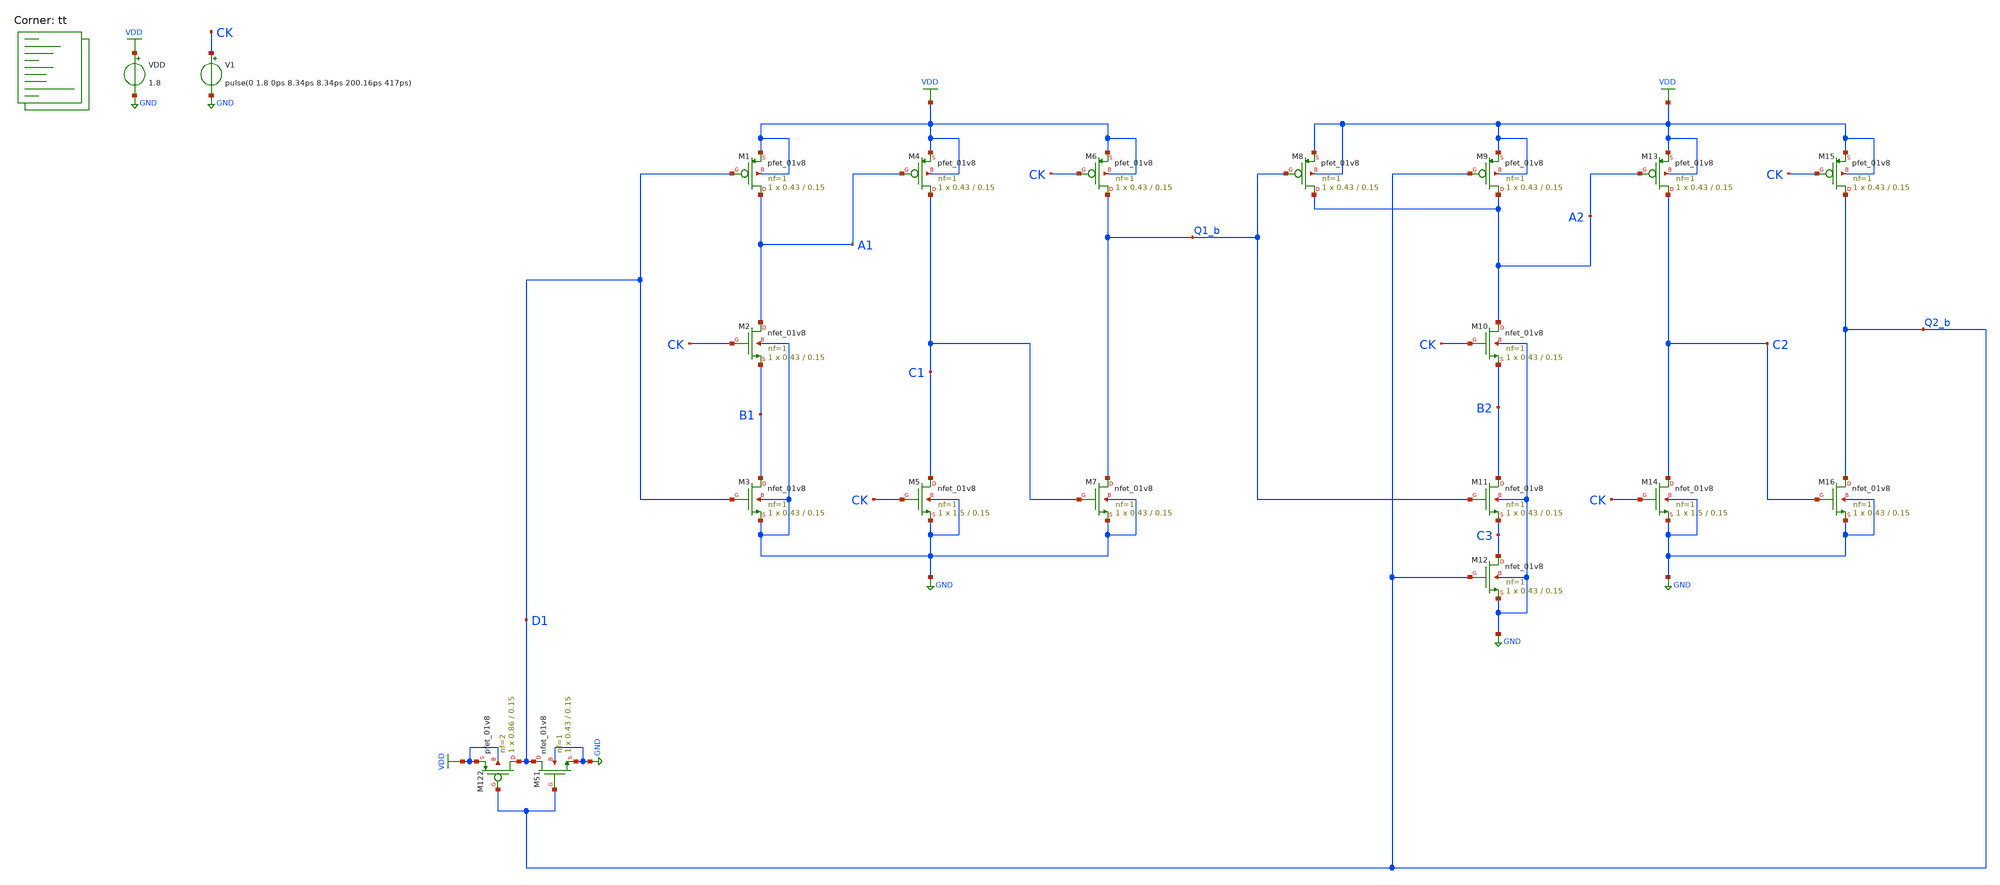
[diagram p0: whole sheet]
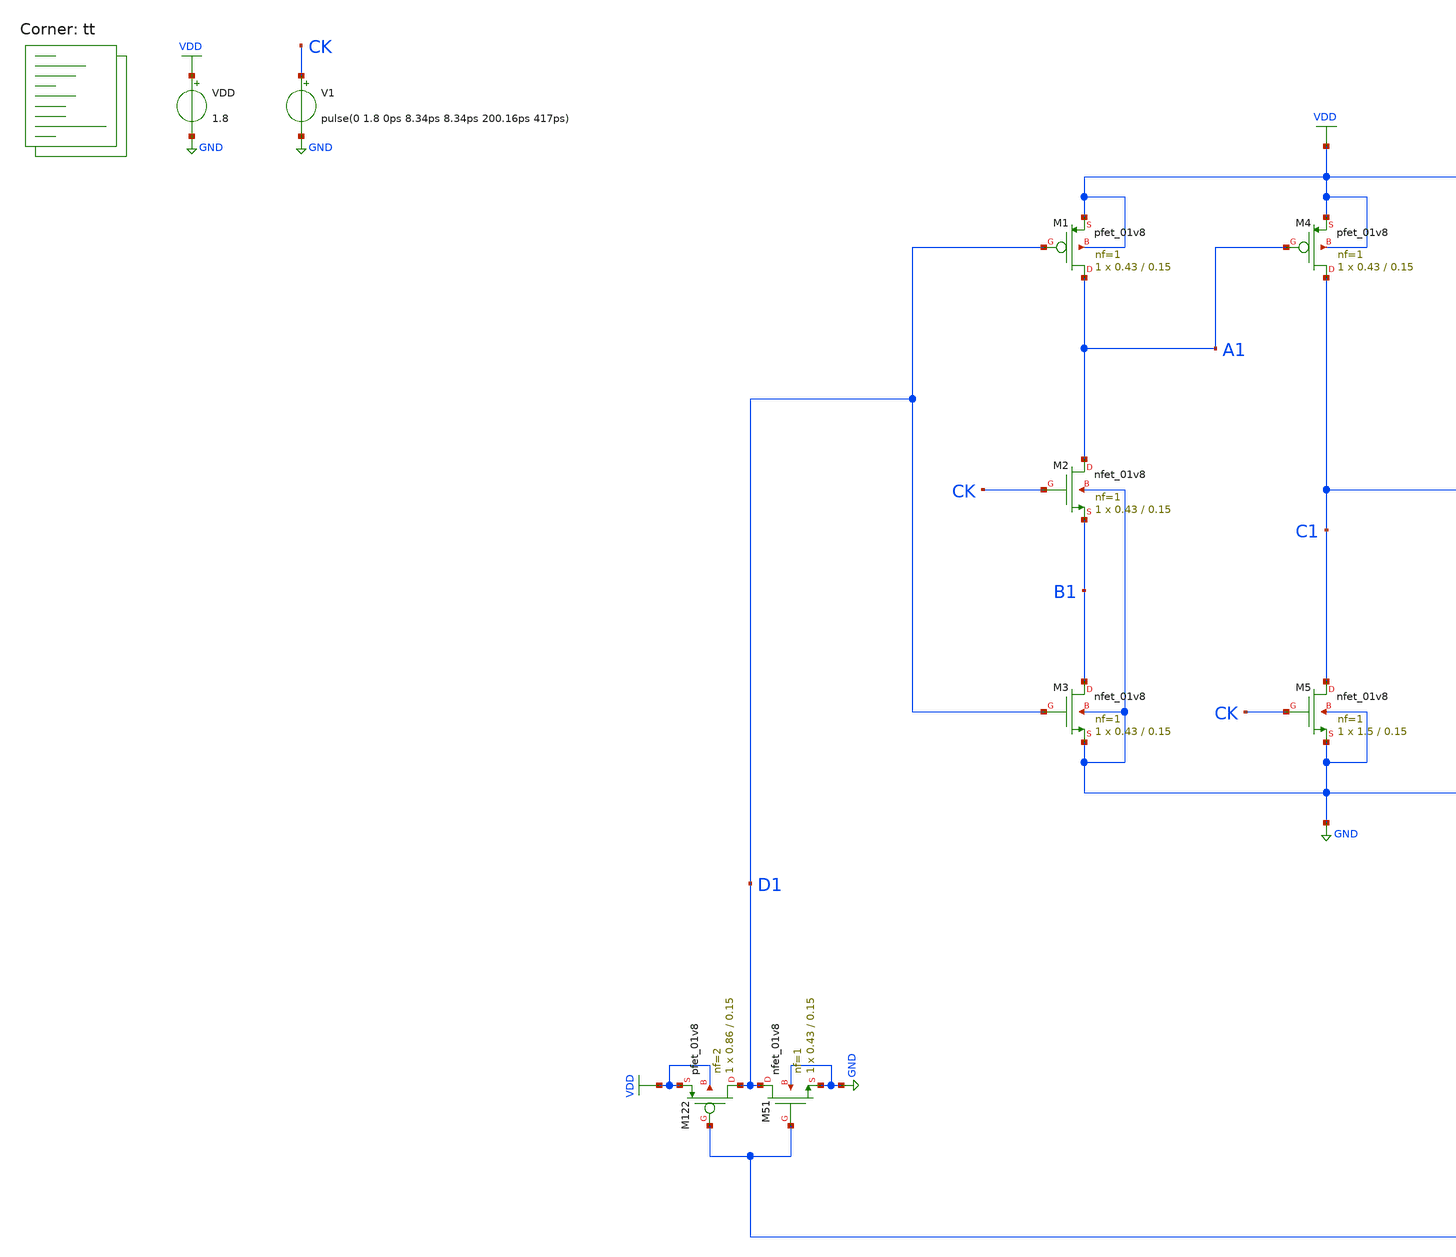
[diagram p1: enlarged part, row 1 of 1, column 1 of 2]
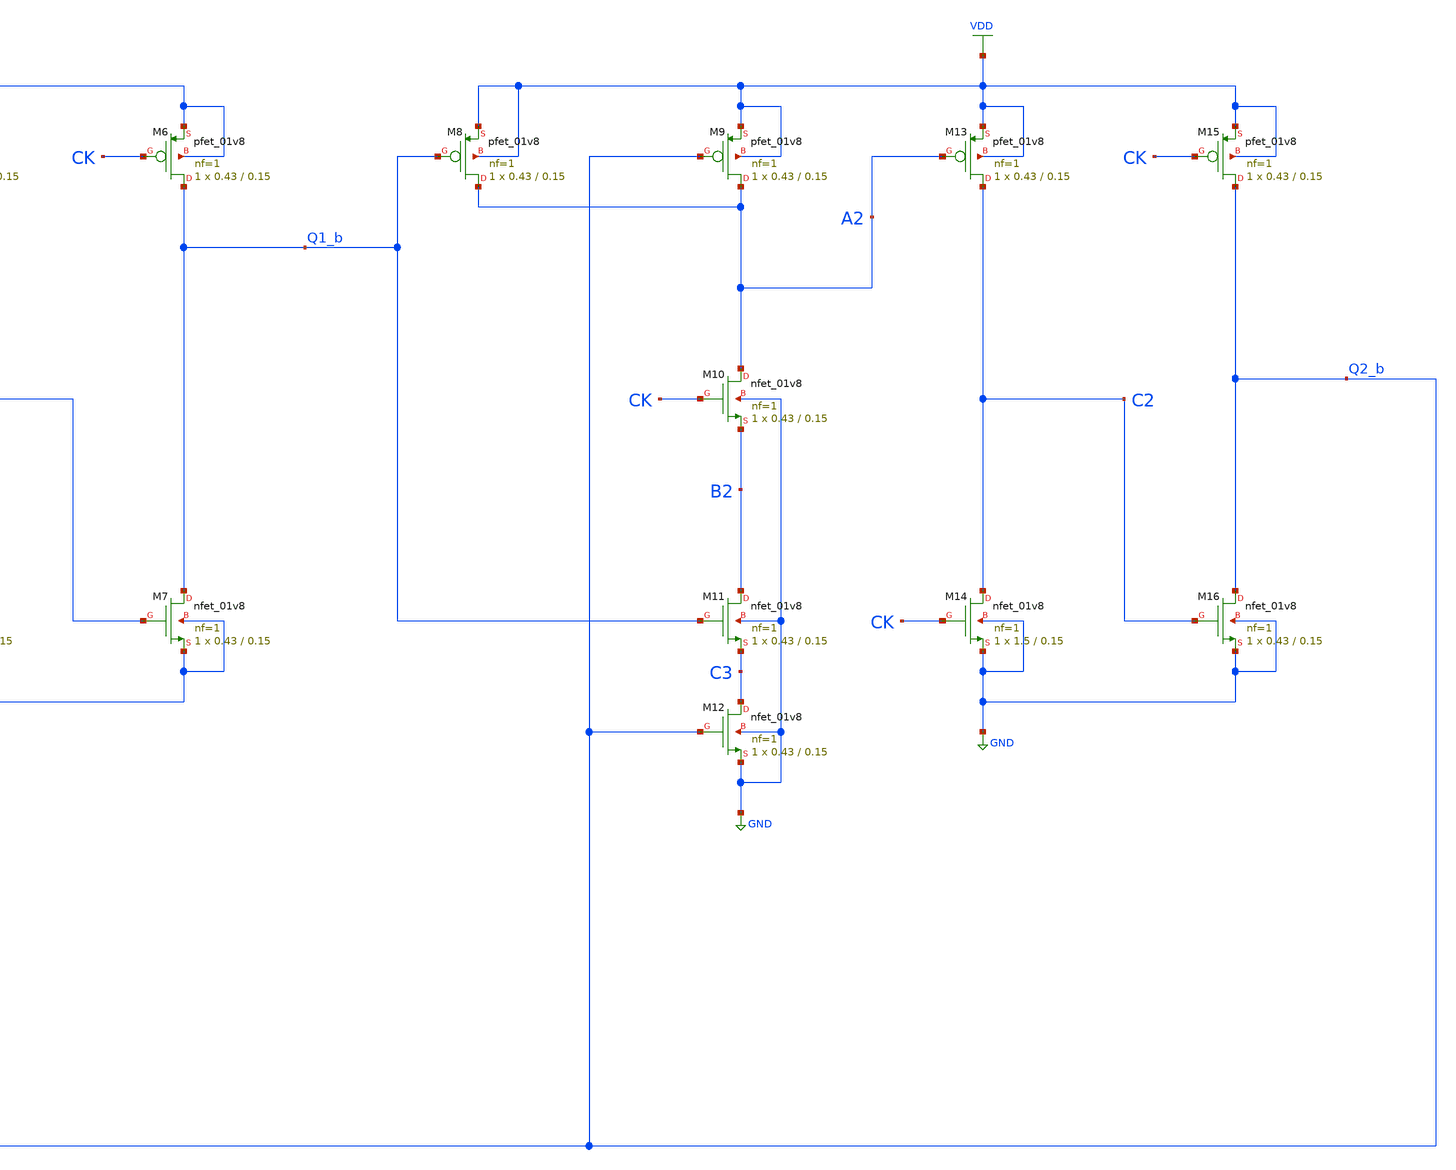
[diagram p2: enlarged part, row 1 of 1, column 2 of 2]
** sch_path: projects/pll/divider/xschem_ngspice/tb_TSPC_FF_ratioed_divide3_3.sch
**.subckt tb_TSPC_FF_ratioed_divide3_3
VDD VDD GND 1.8
XM6 Q1_b CK VDD VDD sky130_fd_pr__pfet_01v8 L=0.15 W=0.43 nf=1 ad='int((nf+1)/2) * W/nf * 0.29' as='int((nf+2)/2) * W/nf * 0.29'
+ pd='2*int((nf+1)/2) * (W/nf + 0.29)' ps='2*int((nf+2)/2) * (W/nf + 0.29)' nrd='0.29 / W' nrs='0.29 / W'
+ sa=0 sb=0 sd=0 mult=1 m=1
XM7 Q1_b C1 GND GND sky130_fd_pr__nfet_01v8 L=0.15 W=0.43 nf=1 ad='int((nf+1)/2) * W/nf * 0.29' as='int((nf+2)/2) * W/nf * 0.29'
+ pd='2*int((nf+1)/2) * (W/nf + 0.29)' ps='2*int((nf+2)/2) * (W/nf + 0.29)' nrd='0.29 / W' nrs='0.29 / W'
+ sa=0 sb=0 sd=0 mult=1 m=1
XM4 C1 A1 VDD VDD sky130_fd_pr__pfet_01v8 L=0.15 W=0.43 nf=1 ad='int((nf+1)/2) * W/nf * 0.29' as='int((nf+2)/2) * W/nf * 0.29'
+ pd='2*int((nf+1)/2) * (W/nf + 0.29)' ps='2*int((nf+2)/2) * (W/nf + 0.29)' nrd='0.29 / W' nrs='0.29 / W'
+ sa=0 sb=0 sd=0 mult=1 m=1
XM5 C1 CK GND GND sky130_fd_pr__nfet_01v8 L=0.15 W=1.5 nf=1 ad='int((nf+1)/2) * W/nf * 0.29' as='int((nf+2)/2) * W/nf * 0.29'
+ pd='2*int((nf+1)/2) * (W/nf + 0.29)' ps='2*int((nf+2)/2) * (W/nf + 0.29)' nrd='0.29 / W' nrs='0.29 / W'
+ sa=0 sb=0 sd=0 mult=1 m=1
XM1 A1 D1 VDD VDD sky130_fd_pr__pfet_01v8 L=0.15 W=0.43 nf=1 ad='int((nf+1)/2) * W/nf * 0.29' as='int((nf+2)/2) * W/nf * 0.29'
+ pd='2*int((nf+1)/2) * (W/nf + 0.29)' ps='2*int((nf+2)/2) * (W/nf + 0.29)' nrd='0.29 / W' nrs='0.29 / W'
+ sa=0 sb=0 sd=0 mult=1 m=1
XM3 B1 D1 GND GND sky130_fd_pr__nfet_01v8 L=0.15 W=0.43 nf=1 ad='int((nf+1)/2) * W/nf * 0.29' as='int((nf+2)/2) * W/nf * 0.29'
+ pd='2*int((nf+1)/2) * (W/nf + 0.29)' ps='2*int((nf+2)/2) * (W/nf + 0.29)' nrd='0.29 / W' nrs='0.29 / W'
+ sa=0 sb=0 sd=0 mult=1 m=1
XM2 A1 CK B1 GND sky130_fd_pr__nfet_01v8 L=0.15 W=0.43 nf=1 ad='int((nf+1)/2) * W/nf * 0.29' as='int((nf+2)/2) * W/nf * 0.29'
+ pd='2*int((nf+1)/2) * (W/nf + 0.29)' ps='2*int((nf+2)/2) * (W/nf + 0.29)' nrd='0.29 / W' nrs='0.29 / W'
+ sa=0 sb=0 sd=0 mult=1 m=1
XM15 Q2_b CK VDD VDD sky130_fd_pr__pfet_01v8 L=0.15 W=0.43 nf=1 ad='int((nf+1)/2) * W/nf * 0.29' as='int((nf+2)/2) * W/nf * 0.29'
+ pd='2*int((nf+1)/2) * (W/nf + 0.29)' ps='2*int((nf+2)/2) * (W/nf + 0.29)' nrd='0.29 / W' nrs='0.29 / W'
+ sa=0 sb=0 sd=0 mult=1 m=1
XM16 Q2_b C2 GND GND sky130_fd_pr__nfet_01v8 L=0.15 W=0.43 nf=1 ad='int((nf+1)/2) * W/nf * 0.29' as='int((nf+2)/2) * W/nf * 0.29'
+ pd='2*int((nf+1)/2) * (W/nf + 0.29)' ps='2*int((nf+2)/2) * (W/nf + 0.29)' nrd='0.29 / W' nrs='0.29 / W'
+ sa=0 sb=0 sd=0 mult=1 m=1
XM13 C2 A2 VDD VDD sky130_fd_pr__pfet_01v8 L=0.15 W=0.43 nf=1 ad='int((nf+1)/2) * W/nf * 0.29' as='int((nf+2)/2) * W/nf * 0.29'
+ pd='2*int((nf+1)/2) * (W/nf + 0.29)' ps='2*int((nf+2)/2) * (W/nf + 0.29)' nrd='0.29 / W' nrs='0.29 / W'
+ sa=0 sb=0 sd=0 mult=1 m=1
XM14 C2 CK GND GND sky130_fd_pr__nfet_01v8 L=0.15 W=1.5 nf=1 ad='int((nf+1)/2) * W/nf * 0.29' as='int((nf+2)/2) * W/nf * 0.29'
+ pd='2*int((nf+1)/2) * (W/nf + 0.29)' ps='2*int((nf+2)/2) * (W/nf + 0.29)' nrd='0.29 / W' nrs='0.29 / W'
+ sa=0 sb=0 sd=0 mult=1 m=1
XM9 A2 Q2_b VDD VDD sky130_fd_pr__pfet_01v8 L=0.15 W=0.43 nf=1 ad='int((nf+1)/2) * W/nf * 0.29' as='int((nf+2)/2) * W/nf * 0.29'
+ pd='2*int((nf+1)/2) * (W/nf + 0.29)' ps='2*int((nf+2)/2) * (W/nf + 0.29)' nrd='0.29 / W' nrs='0.29 / W'
+ sa=0 sb=0 sd=0 mult=1 m=1
XM11 B2 Q1_b C3 GND sky130_fd_pr__nfet_01v8 L=0.15 W=0.43 nf=1 ad='int((nf+1)/2) * W/nf * 0.29' as='int((nf+2)/2) * W/nf * 0.29'
+ pd='2*int((nf+1)/2) * (W/nf + 0.29)' ps='2*int((nf+2)/2) * (W/nf + 0.29)' nrd='0.29 / W' nrs='0.29 / W'
+ sa=0 sb=0 sd=0 mult=1 m=1
XM10 A2 CK B2 GND sky130_fd_pr__nfet_01v8 L=0.15 W=0.43 nf=1 ad='int((nf+1)/2) * W/nf * 0.29' as='int((nf+2)/2) * W/nf * 0.29'
+ pd='2*int((nf+1)/2) * (W/nf + 0.29)' ps='2*int((nf+2)/2) * (W/nf + 0.29)' nrd='0.29 / W' nrs='0.29 / W'
+ sa=0 sb=0 sd=0 mult=1 m=1
V1 CK GND pulse(0 1.8 0ps 8.34ps 8.34ps 200.16ps 417ps)
XM122 D1 Q2_b VDD VDD sky130_fd_pr__pfet_01v8 L=0.15 W=0.86 nf=2 ad='int((nf+1)/2) * W/nf * 0.29' as='int((nf+2)/2) * W/nf * 0.29'
+ pd='2*int((nf+1)/2) * (W/nf + 0.29)' ps='2*int((nf+2)/2) * (W/nf + 0.29)' nrd='0.29 / W' nrs='0.29 / W'
+ sa=0 sb=0 sd=0 mult=1 m=1
XM51 D1 Q2_b GND GND sky130_fd_pr__nfet_01v8 L=0.15 W=0.43 nf=1 ad='int((nf+1)/2) * W/nf * 0.29' as='int((nf+2)/2) * W/nf * 0.29'
+ pd='2*int((nf+1)/2) * (W/nf + 0.29)' ps='2*int((nf+2)/2) * (W/nf + 0.29)' nrd='0.29 / W' nrs='0.29 / W'
+ sa=0 sb=0 sd=0 mult=1 m=1
XM12 C3 Q2_b GND GND sky130_fd_pr__nfet_01v8 L=0.15 W=0.43 nf=1 ad='int((nf+1)/2) * W/nf * 0.29' as='int((nf+2)/2) * W/nf * 0.29'
+ pd='2*int((nf+1)/2) * (W/nf + 0.29)' ps='2*int((nf+2)/2) * (W/nf + 0.29)' nrd='0.29 / W' nrs='0.29 / W'
+ sa=0 sb=0 sd=0 mult=1 m=1
XM8 A2 Q1_b VDD VDD sky130_fd_pr__pfet_01v8 L=0.15 W=0.43 nf=1 ad='int((nf+1)/2) * W/nf * 0.29' as='int((nf+2)/2) * W/nf * 0.29'
+ pd='2*int((nf+1)/2) * (W/nf + 0.29)' ps='2*int((nf+2)/2) * (W/nf + 0.29)' nrd='0.29 / W' nrs='0.29 / W'
+ sa=0 sb=0 sd=0 mult=1 m=1
**** begin user architecture code



.option method=gear
.option wnflag=1

.control

  save all
  tran 5p 20n
  remzerovec
  write tb_TSPC_FF_ratioed_divide3_3.raw
  set appendwrite

.endc



.lib $::SKYWATER_MODELS/sky130.lib.spice tt
**** end user architecture code
**.ends
.GLOBAL GND
.GLOBAL VDD
.end
